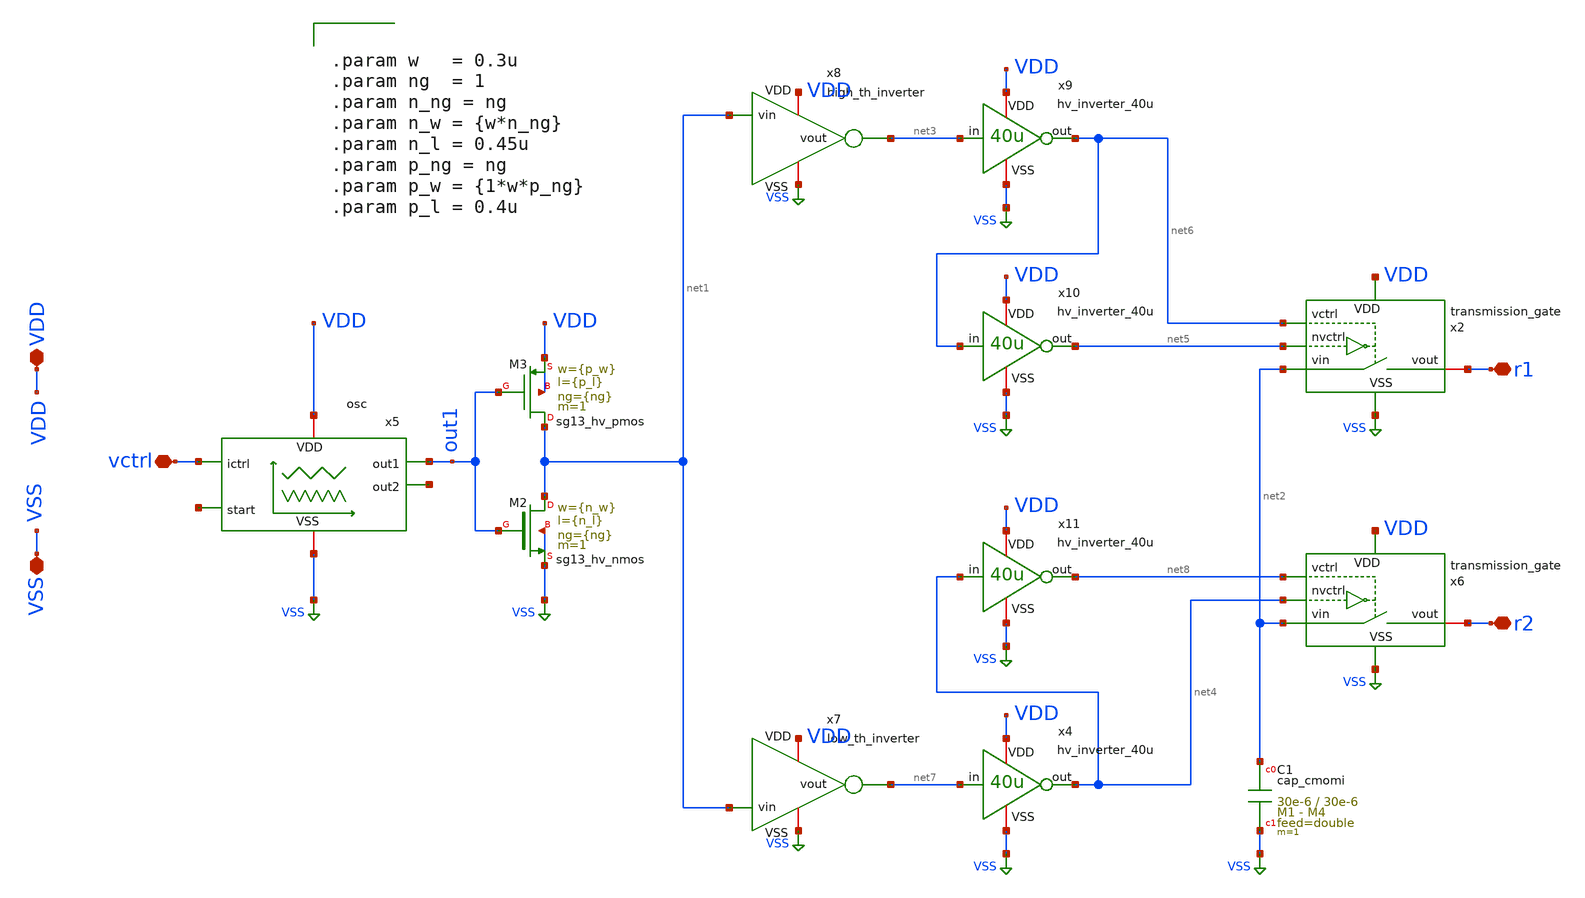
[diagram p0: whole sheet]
** sch_path: macros/heichips26_vcr/macros/switched_capacitor/schematic/xschem/switched_cap_cell.sch
**.subckt switched_cap_cell r1 r2 VDD VSS vctrl
*.iopin r1
*.iopin r2
*.iopin VDD
*.iopin VSS
*.iopin vctrl
XC1 net2 VSS cap_cmomi w=30e-6 l=30e-6 mmin=1 mmax=4 feed=double subblock=0 m=1 mm_ok=1
XM2 net1 out1 VSS VSS sg13_hv_nmos w={n_w} l={n_l} ng={ng} m=1 mm_ok=1
XM3 net1 out1 VDD VDD sg13_hv_pmos w={p_w} l={p_l} ng={ng} m=1 mm_ok=1
x2 net6 net2 r1 net5 VDD VSS transmission_gate
x4 VDD net7 net4 VSS hv_inverter_40u
x5 VDD out1 vctrl VSS net9 net10 osc
x6 net8 net2 r2 net4 VDD VSS transmission_gate
x7 VDD net1 net7 VSS low_th_inverter
x8 VDD net1 net3 VSS high_th_inverter
x9 VDD net3 net6 VSS hv_inverter_40u
x10 VDD net6 net5 VSS hv_inverter_40u
x11 VDD net4 net8 VSS hv_inverter_40u
**** begin user architecture code


.param w   = 0.3u
.param ng  = 1
.param n_ng = ng
.param n_w = {w*n_ng}
.param n_l = 0.45u
.param p_ng = ng
.param p_w = {1*w*p_ng}
.param p_l = 0.4u


**** end user architecture code
**.ends

* expanding   symbol:  transmission_gate.sym # of pins=6
** sym_path: macros/heichips26_vcr/macros/switched_capacitor/schematic/xschem/transmission_gate.sym
** sch_path: macros/heichips26_vcr/macros/switched_capacitor/schematic/xschem/transmission_gate.sch
.subckt transmission_gate vctrl vin vout nvctrl VDD VSS
*.iopin vin
*.iopin vout
*.ipin vctrl
*.ipin nvctrl
*.iopin VDD
*.iopin VSS
XM3 vout vctrl vin VSS sg13_hv_nmos w={tg_ngate_w*tg_ng} l={tg_ch_len} ng={tg_ng} m=1 mm_ok=1
XM4 vout nvctrl vin VDD sg13_hv_pmos w={tg_pgate_w*tg_ng} l={tg_ch_len} ng={tg_ng} m=1 mm_ok=1
**** begin user architecture code


.param tg_ch_len=1u
.param tg_ngate_w=2u
.param tg_pgate_w=10u
.param tg_ng=20


**** end user architecture code
.ends


* expanding   symbol:  hv_inverter_40u.sym # of pins=4
** sym_path: macros/heichips26_vcr/macros/switched_capacitor/schematic/xschem/hv_inverter_40u.sym
** sch_path: macros/heichips26_vcr/macros/switched_capacitor/schematic/xschem/hv_inverter_40u.sch
.subckt hv_inverter_40u VDD in out VSS
*.ipin in
*.iopin VDD
*.iopin VSS
*.opin out
XM2 out in VSS VSS sg13_hv_nmos w={n_w} l={n_l} ng={ng} m=1 mm_ok=1
XM3 out in VDD VDD sg13_hv_pmos w={p_w} l={p_l} ng={ng} m=1 mm_ok=1
**** begin user architecture code


.param w   = 10u
.param ng  = 4
.param n_ng = ng
.param n_w = {3u*n_ng}
.param n_l = 0.45u
.param p_ng = ng
.param p_w = {10u*p_ng}
.param p_l = 0.4u


**** end user architecture code
.ends


* expanding   symbol:  osc.sym # of pins=6
** sym_path: macros/heichips26_vcr/macros/switched_capacitor/schematic/xschem/osc.sym
** sch_path: macros/heichips26_vcr/macros/switched_capacitor/schematic/xschem/osc.sch
.subckt osc VDD out1 ictrl VSS start out2
*.iopin VSS
*.iopin VDD
*.iopin out2
*.iopin out1
*.iopin start
*.iopin ictrl
XM3 out1 ictrl VDD VDD sg13_hv_pmos w=10.0u l=2.0u ng=1 m=1 mm_ok=1
XM2 net1 ictrl VDD VDD sg13_hv_pmos w=1u l=2.0u ng=1 m=1 mm_ok=1
XM4 start ictrl VDD VDD sg13_hv_pmos w=1.0u l=2.0u ng=1 m=1 mm_ok=1
XM5 out2 ictrl VDD VDD sg13_hv_pmos w=10.0u l=2.0u ng=1 m=1 mm_ok=1
XM6 ictrl ictrl VDD VDD sg13_hv_pmos w=10.0u l=2.0u ng=1 m=1 mm_ok=1
XC1 net1 out1 cap_cmomi w=10e-6 l=10e-6 mmin=1 mmax=4 feed=double subblock=0 m=1 mm_ok=1
XC2 out2 start cap_cmomi w=10e-6 l=10e-6 mmin=1 mmax=4 feed=double subblock=0 m=1 mm_ok=1
XM8 out1 start VSS VSS sg13_hv_nmos w=3u l=0.45u ng=1 m=1 mm_ok=1
XM1 start start VSS VSS sg13_hv_nmos w=1u l=2u ng=1 m=1 mm_ok=1
XM12 out2 net1 VSS VSS sg13_hv_nmos w=3u l=0.45u ng=1 m=1 mm_ok=1
XM11 net1 net1 VSS VSS sg13_hv_nmos w=1u l=2u ng=1 m=1 mm_ok=1
**** begin user architecture code


.ic v(out1)=0 v(out2)=3.3


**** end user architecture code
.ends


* expanding   symbol:  low_th_inverter.sym # of pins=4
** sym_path: macros/heichips26_vcr/macros/switched_capacitor/schematic/xschem/low_th_inverter.sym
** sch_path: macros/heichips26_vcr/macros/switched_capacitor/schematic/xschem/low_th_inverter.sch
.subckt low_th_inverter VDD vin vout VSS
*.ipin vin
*.iopin VDD
*.iopin VSS
*.opin vout
XM1 vout vin VSS VSS sg13_hv_nmos w={n_ng*n_w} l={n_l} ng={n_ng} m=1 mm_ok=1
XM2 vout vin VDD VDD sg13_hv_pmos w={p_ng*p_w} l={p_l} ng={n_ng} m=1 mm_ok=1
**** begin user architecture code


.param n_ng = 2
.param n_w = 1u
.param n_l = 0.45u
.param p_ng = 2
.param p_w = 1u
.param p_l = 0.4u


**** end user architecture code
.ends


* expanding   symbol:  high_th_inverter.sym # of pins=4
** sym_path: macros/heichips26_vcr/macros/switched_capacitor/schematic/xschem/high_th_inverter.sym
** sch_path: macros/heichips26_vcr/macros/switched_capacitor/schematic/xschem/high_th_inverter.sch
.subckt high_th_inverter VDD vin vout VSS
*.ipin vin
*.iopin VDD
*.iopin VSS
*.opin vout
XMdummy1 VSS VSS VSS VSS sg13_hv_nmos w=0.6u l=1.0u ng=2 m=1 mm_ok=1
XMdummy2 VDD VDD VDD VDD sg13_hv_pmos w=12.0u l=1.0u ng=2 m=1 mm_ok=1
XM1 vout vin VSS VSS sg13_hv_nmos w=6.0u l=1.0u ng=20 m=1 mm_ok=1
XM2 vout vin VDD VDD sg13_hv_pmos w=120.0u l=1.0u ng=20 m=1 mm_ok=1
.ends

.GLOBAL VSS
.end
